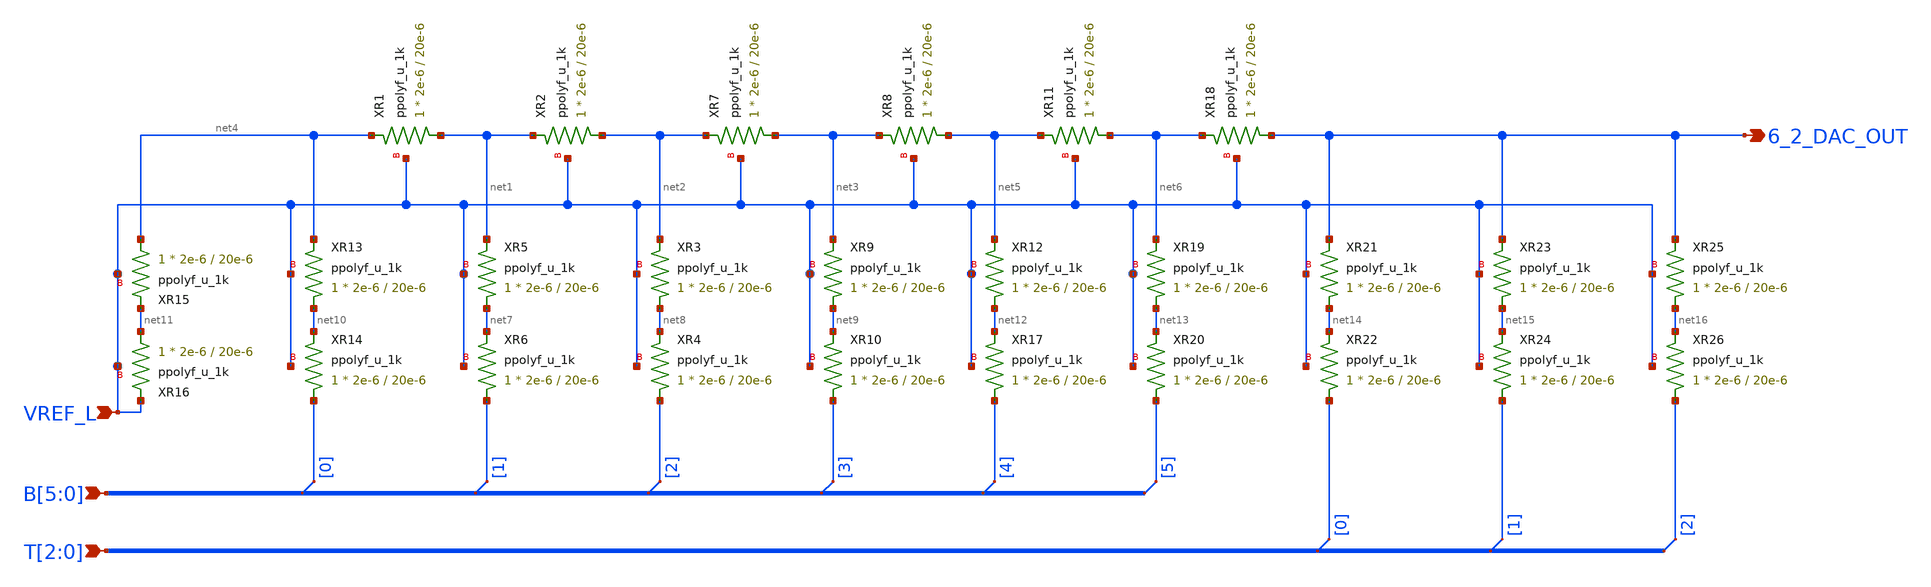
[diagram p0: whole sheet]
** sch_path: xschem/6_2_dac.sch
**.subckt 6_2_dac VREF_L B[5],B[4],B[3],B[2],B[1],B[0] T[2],T[1],T[0] 6_2_DAC_OUT
*.ipin VREF_L
*.ipin B[5],B[4],B[3],B[2],B[1],B[0]
*.ipin T[2],T[1],T[0]
*.opin 6_2_DAC_OUT
XR1 net1 net4 VREF_L ppolyf_u_1k r_width=2e-6 r_length=20e-6 m=1
XR2 net2 net1 VREF_L ppolyf_u_1k r_width=2e-6 r_length=20e-6 m=1
XR5 net7 net1 VREF_L ppolyf_u_1k r_width=2e-6 r_length=20e-6 m=1
XR6 B[1] net7 VREF_L ppolyf_u_1k r_width=2e-6 r_length=20e-6 m=1
XR3 net8 net2 VREF_L ppolyf_u_1k r_width=2e-6 r_length=20e-6 m=1
XR4 B[2] net8 VREF_L ppolyf_u_1k r_width=2e-6 r_length=20e-6 m=1
XR7 net3 net2 VREF_L ppolyf_u_1k r_width=2e-6 r_length=20e-6 m=1
XR8 net5 net3 VREF_L ppolyf_u_1k r_width=2e-6 r_length=20e-6 m=1
XR9 net9 net3 VREF_L ppolyf_u_1k r_width=2e-6 r_length=20e-6 m=1
XR10 B[3] net9 VREF_L ppolyf_u_1k r_width=2e-6 r_length=20e-6 m=1
XR13 net10 net4 VREF_L ppolyf_u_1k r_width=2e-6 r_length=20e-6 m=1
XR14 B[0] net10 VREF_L ppolyf_u_1k r_width=2e-6 r_length=20e-6 m=1
XR15 net4 net11 VREF_L ppolyf_u_1k r_width=2e-6 r_length=20e-6 m=1
XR16 net11 VREF_L VREF_L ppolyf_u_1k r_width=2e-6 r_length=20e-6 m=1
XR11 net6 net5 VREF_L ppolyf_u_1k r_width=2e-6 r_length=20e-6 m=1
XR12 net12 net5 VREF_L ppolyf_u_1k r_width=2e-6 r_length=20e-6 m=1
XR17 B[4] net12 VREF_L ppolyf_u_1k r_width=2e-6 r_length=20e-6 m=1
* tap: B[5:0] --> B[0]
* tap: B[5:0] --> B[1]
* tap: B[5:0] --> B[2]
* tap: B[5:0] --> B[3]
* tap: B[5:0] --> B[4]
XR18 6_2_DAC_OUT net6 VREF_L ppolyf_u_1k r_width=2e-6 r_length=20e-6 m=1
XR19 net13 net6 VREF_L ppolyf_u_1k r_width=2e-6 r_length=20e-6 m=1
XR20 B[5] net13 VREF_L ppolyf_u_1k r_width=2e-6 r_length=20e-6 m=1
* tap: B[5:0] --> B[5]
XR21 net14 6_2_DAC_OUT VREF_L ppolyf_u_1k r_width=2e-6 r_length=20e-6 m=1
XR22 T[0] net14 VREF_L ppolyf_u_1k r_width=2e-6 r_length=20e-6 m=1
XR23 net15 6_2_DAC_OUT VREF_L ppolyf_u_1k r_width=2e-6 r_length=20e-6 m=1
XR24 T[1] net15 VREF_L ppolyf_u_1k r_width=2e-6 r_length=20e-6 m=1
XR25 net16 6_2_DAC_OUT VREF_L ppolyf_u_1k r_width=2e-6 r_length=20e-6 m=1
XR26 T[2] net16 VREF_L ppolyf_u_1k r_width=2e-6 r_length=20e-6 m=1
* tap: T[2:0] --> T[0]
* tap: T[2:0] --> T[1]
* tap: T[2:0] --> T[2]
**.ends
.end
